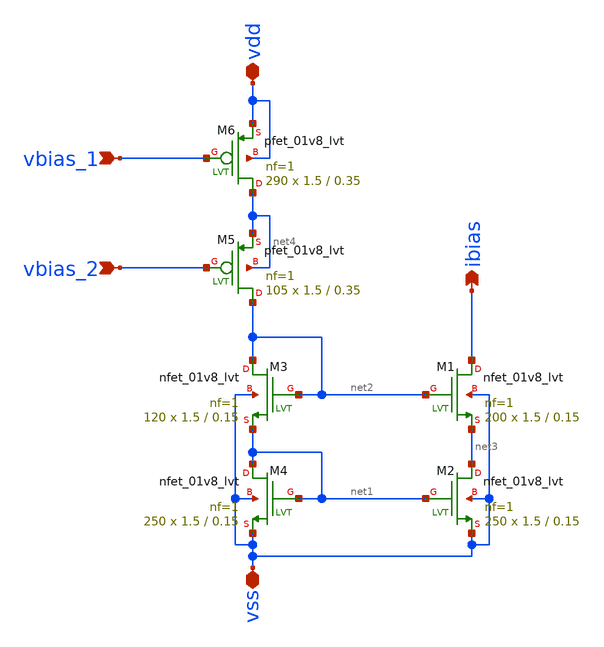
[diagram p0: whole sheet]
** sch_path: track_analogico/bias/sch/bias.sch
**.subckt bias vdd vss ibias vbias_1 vbias_2
*.iopin vdd
*.iopin vss
*.opin ibias
*.ipin vbias_1
*.ipin vbias_2
XM1 ibias net2 net3 vss sky130_fd_pr__nfet_01v8_lvt L=0.15 W=1.5 nf=1 ad='int((nf+1)/2) * W/nf * 0.29'
+ as='int((nf+2)/2) * W/nf * 0.29' pd='2*int((nf+1)/2) * (W/nf + 0.29)' ps='2*int((nf+2)/2) * (W/nf + 0.29)'
+ nrd='0.29 / W' nrs='0.29 / W' sa=0 sb=0 sd=0 mult=200 m=200
XM2 net3 net1 vss vss sky130_fd_pr__nfet_01v8_lvt L=0.15 W=1.5 nf=1 ad='int((nf+1)/2) * W/nf * 0.29'
+ as='int((nf+2)/2) * W/nf * 0.29' pd='2*int((nf+1)/2) * (W/nf + 0.29)' ps='2*int((nf+2)/2) * (W/nf + 0.29)'
+ nrd='0.29 / W' nrs='0.29 / W' sa=0 sb=0 sd=0 mult=250 m=250
XM3 net2 net2 net1 vss sky130_fd_pr__nfet_01v8_lvt L=0.15 W=1.5 nf=1 ad='int((nf+1)/2) * W/nf * 0.29'
+ as='int((nf+2)/2) * W/nf * 0.29' pd='2*int((nf+1)/2) * (W/nf + 0.29)' ps='2*int((nf+2)/2) * (W/nf + 0.29)'
+ nrd='0.29 / W' nrs='0.29 / W' sa=0 sb=0 sd=0 mult=120 m=120
XM4 net1 net1 vss vss sky130_fd_pr__nfet_01v8_lvt L=0.15 W=1.5 nf=1 ad='int((nf+1)/2) * W/nf * 0.29'
+ as='int((nf+2)/2) * W/nf * 0.29' pd='2*int((nf+1)/2) * (W/nf + 0.29)' ps='2*int((nf+2)/2) * (W/nf + 0.29)'
+ nrd='0.29 / W' nrs='0.29 / W' sa=0 sb=0 sd=0 mult=250 m=250
XM5 net2 vbias_2 net4 net4 sky130_fd_pr__pfet_01v8_lvt L=0.35 W=1.5 nf=1 ad='int((nf+1)/2) * W/nf * 0.29'
+ as='int((nf+2)/2) * W/nf * 0.29' pd='2*int((nf+1)/2) * (W/nf + 0.29)' ps='2*int((nf+2)/2) * (W/nf + 0.29)'
+ nrd='0.29 / W' nrs='0.29 / W' sa=0 sb=0 sd=0 mult=105 m=105
XM6 net4 vbias_1 vdd vdd sky130_fd_pr__pfet_01v8_lvt L=0.35 W=1.5 nf=1 ad='int((nf+1)/2) * W/nf * 0.29'
+ as='int((nf+2)/2) * W/nf * 0.29' pd='2*int((nf+1)/2) * (W/nf + 0.29)' ps='2*int((nf+2)/2) * (W/nf + 0.29)'
+ nrd='0.29 / W' nrs='0.29 / W' sa=0 sb=0 sd=0 mult=290 m=290
**.ends
.end
